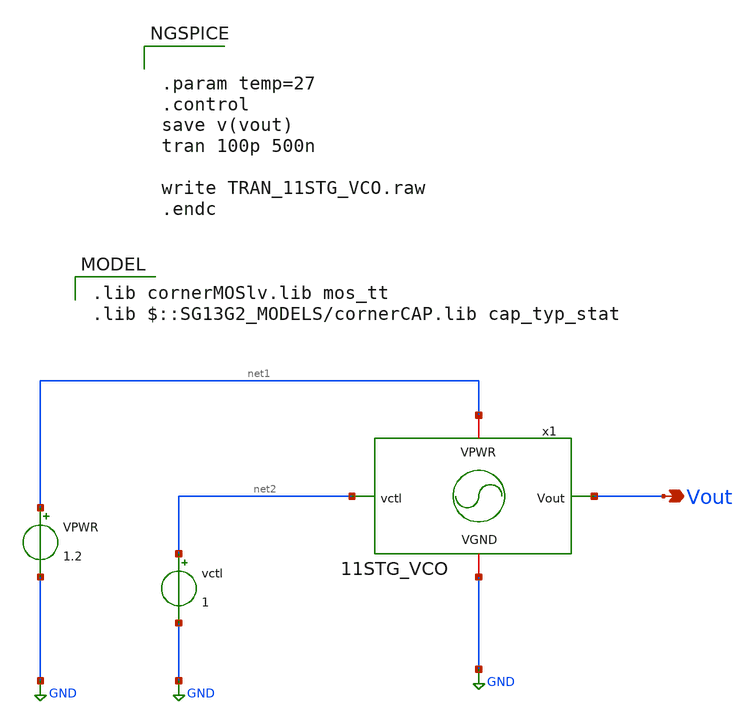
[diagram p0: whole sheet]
** sch_path: 30_MHz_Fractional_N_PLL/design_data/xschem/11STG_VCO_TB.sch
**.subckt 11STG_VCO_TB Vout
*.opin Vout
VPWR net1 GND 1.2
vctl net2 GND 1
x1 net1 GND net2 Vout 11STG_VCO
**** begin user architecture code
 .lib cornerMOSlv.lib mos_tt
.lib $::SG13G2_MODELS/cornerCAP.lib cap_typ_stat



.param temp=27
.control
save v(vout)
tran 100p 500n

write TRAN_11STG_VCO.raw
.endc


**** end user architecture code
**.ends

* expanding   symbol:  11STG_VCO.sym # of pins=4
** sym_path: 30_MHz_Fractional_N_PLL/design_data/xschem/11STG_VCO.sym
** sch_path: 30_MHz_Fractional_N_PLL/design_data/xschem/11STG_VCO.sch
.subckt 11STG_VCO VPWR VGND vctl Vout
*.iopin VPWR
*.iopin VGND
*.ipin vctl
*.opin Vout
XM21 mirror_pg mirror_pg VPWR VPWR sg13_lv_pmos w=0.8u l=0.13u ng=1 m=1 mm_ok=1
XM22 net1 mirror_pg VPWR VPWR sg13_lv_pmos w=0.8u l=0.13u ng=1 m=1 mm_ok=1
XM23 net2 mirror_pg VPWR VPWR sg13_lv_pmos w=0.8u l=0.13u ng=1 m=1 mm_ok=1
XM24 net3 mirror_pg VPWR VPWR sg13_lv_pmos w=0.8u l=0.13u ng=1 m=1 mm_ok=1
XM25 mirror_pg vctl VGND VGND sg13_lv_nmos w=0.6u l=0.13u ng=1 m=1 mm_ok=1
XM26 net9 vctl VGND VGND sg13_lv_nmos w=0.6u l=0.13u ng=1 m=1 mm_ok=1
XM28 net7 vctl VGND VGND sg13_lv_nmos w=0.6u l=0.13u ng=1 m=1 mm_ok=1
XM29 net13 mirror_pg VPWR VPWR sg13_lv_pmos w=0.8u l=0.13u ng=1 m=1 mm_ok=1
XM30 net12 mirror_pg VPWR VPWR sg13_lv_pmos w=0.8u l=0.13u ng=1 m=1 mm_ok=1
XM31 net10 vctl VGND VGND sg13_lv_nmos w=0.6u l=0.13u ng=1 m=1 mm_ok=1
XM32 net11 vctl VGND VGND sg13_lv_nmos w=0.6u l=0.13u ng=1 m=1 mm_ok=1
XM33 net15 mirror_pg VPWR VPWR sg13_lv_pmos w=0.8u l=0.13u ng=1 m=1 mm_ok=1
XM34 net16 mirror_pg VPWR VPWR sg13_lv_pmos w=0.8u l=0.13u ng=1 m=1 mm_ok=1
XM35 net20 vctl VGND VGND sg13_lv_nmos w=0.6u l=0.13u ng=1 m=1 mm_ok=1
XM36 net19 vctl VGND VGND sg13_lv_nmos w=0.6u l=0.13u ng=1 m=1 mm_ok=1
XM37 net24 mirror_pg VPWR VPWR sg13_lv_pmos w=0.8u l=0.13u ng=1 m=1 mm_ok=1
XM38 net23 mirror_pg VPWR VPWR sg13_lv_pmos w=0.8u l=0.13u ng=1 m=1 mm_ok=1
XM39 net21 vctl VGND VGND sg13_lv_nmos w=0.6u l=0.13u ng=1 m=1 mm_ok=1
XM40 net22 vctl VGND VGND sg13_lv_nmos w=0.6u l=0.13u ng=1 m=1 mm_ok=1
XM41 net31 mirror_pg VPWR VPWR sg13_lv_pmos w=0.8u l=0.13u ng=1 m=1 mm_ok=1
XM42 net30 mirror_pg VPWR VPWR sg13_lv_pmos w=0.8u l=0.13u ng=1 m=1 mm_ok=1
XM43 net28 vctl VGND VGND sg13_lv_nmos w=0.6u l=0.13u ng=1 m=1 mm_ok=1
XM44 net29 vctl VGND VGND sg13_lv_nmos w=0.6u l=0.13u ng=1 m=1 mm_ok=1
XM1 net8 vctl VGND VGND sg13_lv_nmos w=0.6u l=0.13u ng=1 m=1 mm_ok=1
XC12 net4 VGND cap_cmim w=6.99e-6 l=6.99e-6 m=1 mm_ok=1
XC1 net5 VGND cap_cmim w=6.99e-6 l=6.99e-6 m=1 mm_ok=1
XC2 net6 VGND cap_cmim w=6.99e-6 l=6.99e-6 m=1 mm_ok=1
XC3 net14 VGND cap_cmim w=6.99e-6 l=6.99e-6 m=1 mm_ok=1
XC4 net26 VGND cap_cmim w=6.99e-6 l=6.99e-6 m=1 mm_ok=1
XC5 net17 VGND cap_cmim w=6.99e-6 l=6.99e-6 m=1 mm_ok=1
XC6 net18 VGND cap_cmim w=6.99e-6 l=6.99e-6 m=1 mm_ok=1
XC7 net25 VGND cap_cmim w=6.99e-6 l=6.99e-6 m=1 mm_ok=1
XC8 net27 VGND cap_cmim w=6.99e-6 l=6.99e-6 m=1 mm_ok=1
XC9 net32 VGND cap_cmim w=6.99e-6 l=6.99e-6 m=1 mm_ok=1
XC10 Vout VGND cap_cmim w=6.99e-6 l=6.99e-6 m=1 mm_ok=1
x1 net1 VPWR Vout net4 VGND net9 VCO_INV
x2 net2 VPWR net4 net5 VGND net8 VCO_INV
x3 net3 VPWR net5 net6 VGND net7 VCO_INV
x4 net13 VPWR net6 net14 VGND net10 VCO_INV
x5 net12 VPWR net14 net26 VGND net11 VCO_INV
x6 net15 VPWR net26 net17 VGND net20 VCO_INV
x7 net16 VPWR net17 net18 VGND net19 VCO_INV
x8 net24 VPWR net18 net25 VGND net21 VCO_INV
x9 net23 VPWR net25 net27 VGND net22 VCO_INV
x10 net31 VPWR net27 net32 VGND net28 VCO_INV
x11 net30 VPWR net32 Vout VGND net29 VCO_INV
.ends


* expanding   symbol:  VCO_INV.sym # of pins=6
** sym_path: 30_MHz_Fractional_N_PLL/design_data/xschem/VCO_INV.sym
** sch_path: 30_MHz_Fractional_N_PLL/design_data/xschem/VCO_INV.sch
.subckt VCO_INV VPWR VPB A Y VNB VGND
*.iopin VPWR
*.iopin VGND
*.ipin A
*.opin Y
*.iopin VPB
*.iopin VNB
XM2 Y A VPWR VPB sg13_lv_pmos w=2u l=0.13u ng=1 m=1 mm_ok=1
XM1 Y A VGND VNB sg13_lv_nmos w=1u l=0.13u ng=1 m=1 mm_ok=1
.ends

.GLOBAL GND
.end
